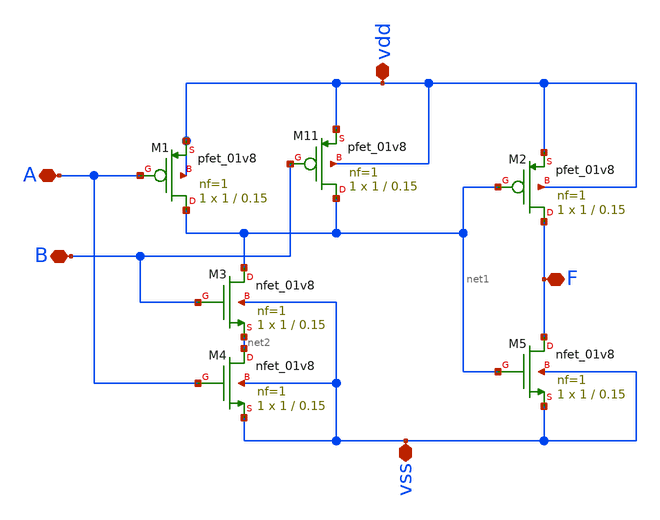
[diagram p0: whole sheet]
** sch_path: practica2/and.sch
**.subckt and A B vdd vss F
*.iopin A
*.iopin B
*.iopin vdd
*.iopin vss
*.iopin F
XM11 net1 B vdd vdd sky130_fd_pr__pfet_01v8 L=0.15 W=1 nf=1 ad='int((nf+1)/2) * W/nf * 0.29' as='int((nf+2)/2) * W/nf * 0.29'
+ pd='2*int((nf+1)/2) * (W/nf + 0.29)' ps='2*int((nf+2)/2) * (W/nf + 0.29)' nrd='0.29 / W' nrs='0.29 / W'
+ sa=0 sb=0 sd=0 mult=1 m=1
XM1 net1 A vdd vdd sky130_fd_pr__pfet_01v8 L=0.15 W=1 nf=1 ad='int((nf+1)/2) * W/nf * 0.29' as='int((nf+2)/2) * W/nf * 0.29'
+ pd='2*int((nf+1)/2) * (W/nf + 0.29)' ps='2*int((nf+2)/2) * (W/nf + 0.29)' nrd='0.29 / W' nrs='0.29 / W'
+ sa=0 sb=0 sd=0 mult=1 m=1
XM2 F net1 vdd vdd sky130_fd_pr__pfet_01v8 L=0.15 W=1 nf=1 ad='int((nf+1)/2) * W/nf * 0.29' as='int((nf+2)/2) * W/nf * 0.29'
+ pd='2*int((nf+1)/2) * (W/nf + 0.29)' ps='2*int((nf+2)/2) * (W/nf + 0.29)' nrd='0.29 / W' nrs='0.29 / W'
+ sa=0 sb=0 sd=0 mult=1 m=1
XM3 net1 B net2 vss sky130_fd_pr__nfet_01v8 L=0.15 W=1 nf=1 ad='int((1 + 1)/2) * 1 / 1 * 0.29' as='int((1 + 2)/2) * 1 / 1 * 0.29'
+ pd='2*int((1 + 1)/2) * (1 / 1 + 0.29)' ps='2*int((1 + 2)/2) * (1 / 1 + 0.29)' nrd='0.29 / 1 ' nrs='0.29 / 1 '
+ sa=0 sb=0 sd=0 mult=1 m=1
XM4 net2 A vss vss sky130_fd_pr__nfet_01v8 L=0.15 W=1 nf=1 ad='int((1 + 1)/2) * 1 / 1 * 0.29' as='int((1 + 2)/2) * 1 / 1 * 0.29'
+ pd='2*int((1 + 1)/2) * (1 / 1 + 0.29)' ps='2*int((1 + 2)/2) * (1 / 1 + 0.29)' nrd='0.29 / 1 ' nrs='0.29 / 1 '
+ sa=0 sb=0 sd=0 mult=1 m=1
XM5 F net1 vss vss sky130_fd_pr__nfet_01v8 L=0.15 W=1 nf=1 ad='int((1 + 1)/2) * 1 / 1 * 0.29' as='int((1 + 2)/2) * 1 / 1 * 0.29'
+ pd='2*int((1 + 1)/2) * (1 / 1 + 0.29)' ps='2*int((1 + 2)/2) * (1 / 1 + 0.29)' nrd='0.29 / 1 ' nrs='0.29 / 1 '
+ sa=0 sb=0 sd=0 mult=1 m=1
**.ends
.end
